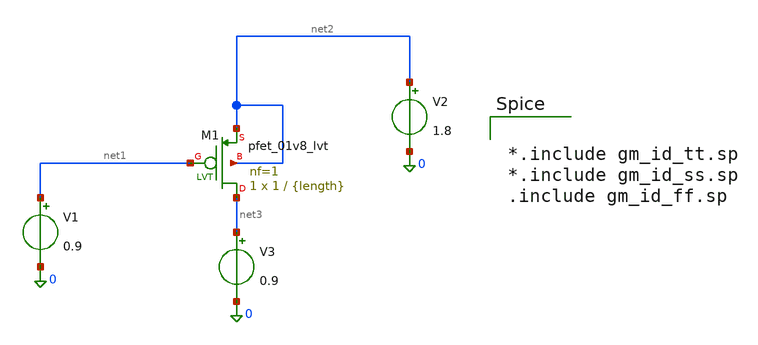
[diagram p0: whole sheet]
** sch_path: xschem/pmos/pmos_lvt_char.sch
**.subckt pmos_lvt_char
V1 net1 0 0.9
V2 net2 0 1.8
XM1 net3 net1 net2 net2 sky130_fd_pr__pfet_01v8_lvt L={length} W=1 nf=1 ad='int((1 + 1)/2) * 1 / 1 * 0.29'
+ as='int((1 + 2)/2) * 1 / 1 * 0.29' pd='2*int((1 + 1)/2) * (1 / 1 + 0.29)' ps='2*int((1 + 2)/2) * (1 / 1 + 0.29)'
+ nrd='0.29 / 1 ' nrs='0.29 / 1 ' sa=0 sb=0 sd=0 mult=1 m=1
V3 net3 0 0.9
**** begin user architecture code


*.include gm_id_tt.sp
*.include gm_id_ss.sp
.include gm_id_ff.sp


**** end user architecture code
**.ends
.end
